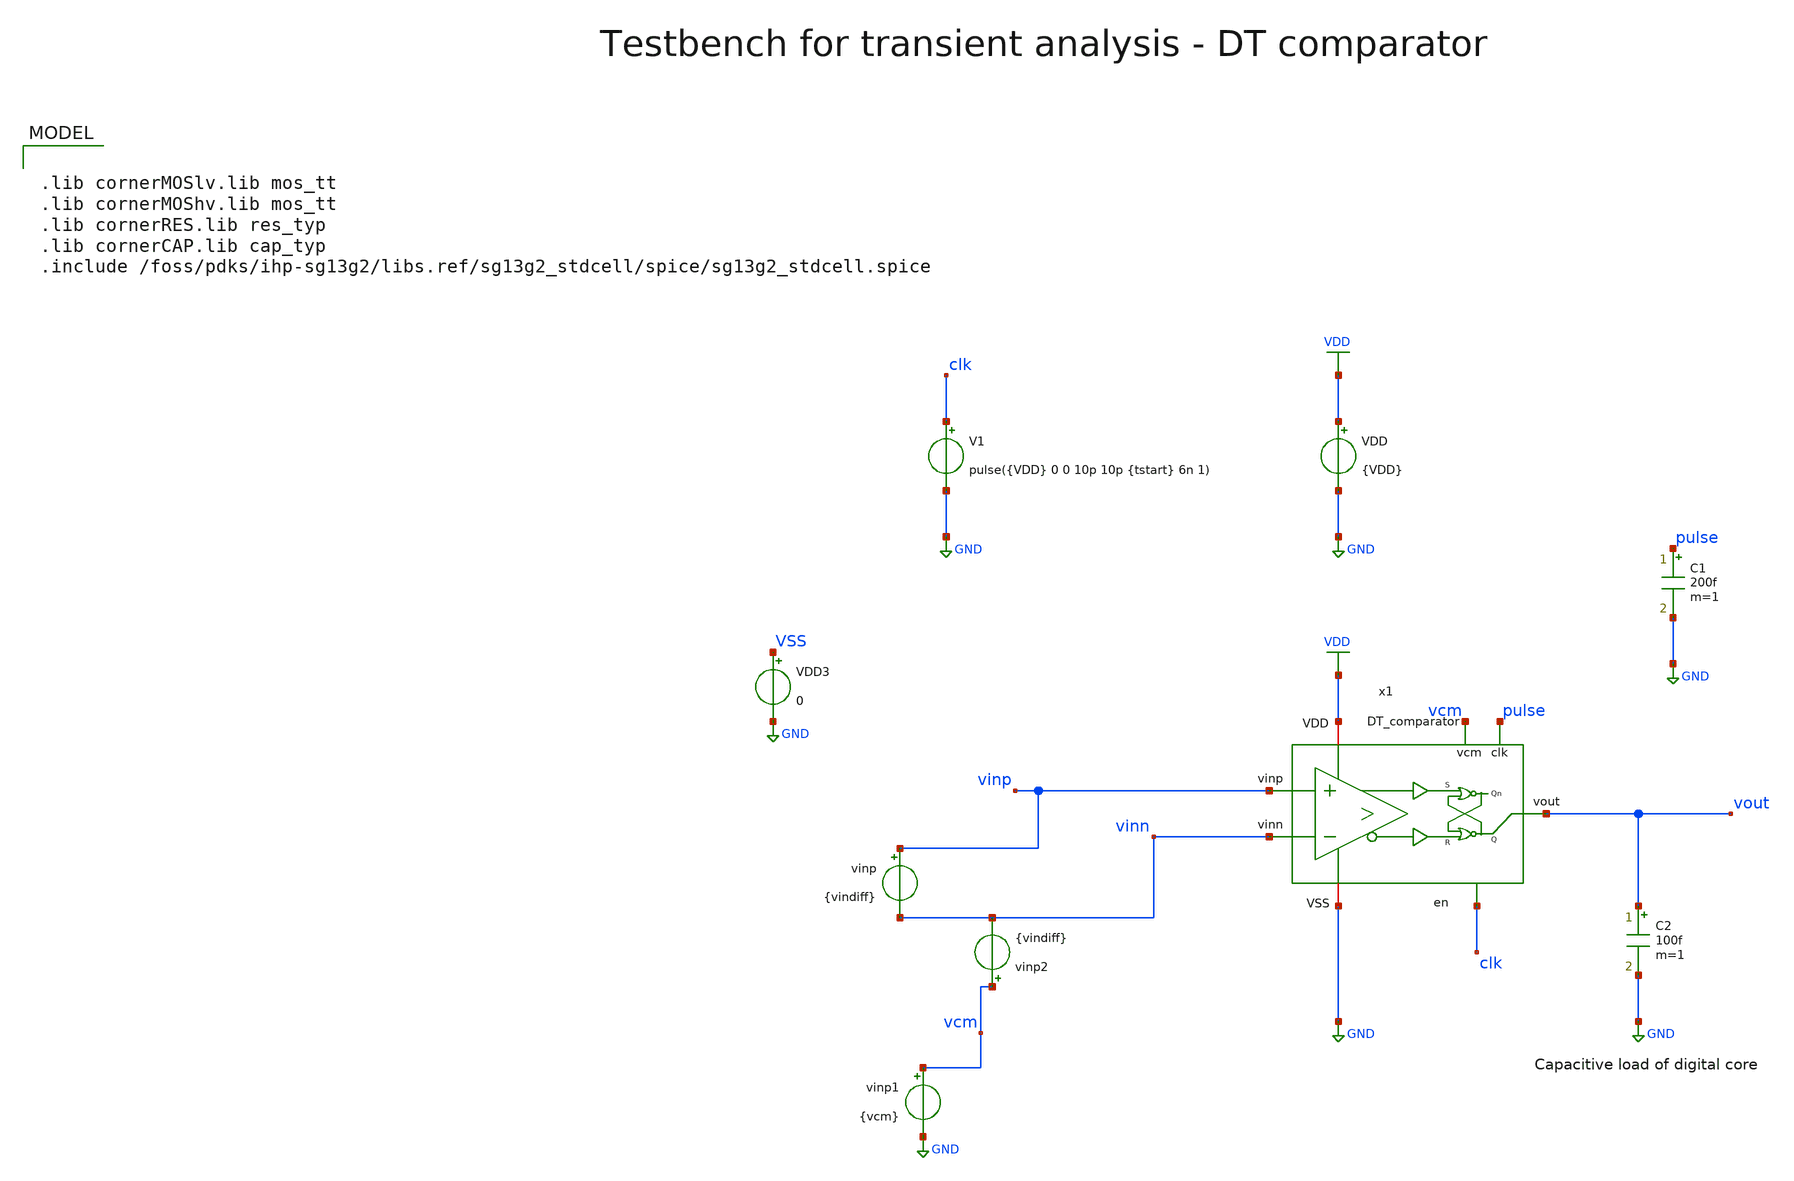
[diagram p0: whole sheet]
** sch_path: xschem/comparator/discrete_time/testbenches/DT_comparator_tb_tran.sch
**.subckt DT_comparator_tb_tran
VDD VDD GND {VDD}
V1 clk GND pulse({VDD} 0 0 10p 10p {tstart} 6n 1)
vinp vinp vinn {vindiff}
C2 vout GND 100f m=1
x1 VDD vinp vout vinn clk GND pulse vcm DT_comparator
VDD3 VSS GND 0
vinp1 vcm GND {vcm}
vinp2 vcm vinn {vindiff}
C1 pulse GND 200f m=1
**** begin user architecture code

.lib cornerMOSlv.lib mos_tt
.lib cornerMOShv.lib mos_tt
.lib cornerRES.lib res_typ
.lib cornerCAP.lib cap_typ
.include /foss/pdks/ihp-sg13g2/libs.ref/sg13g2_stdcell/spice/sg13g2_stdcell.spice



.param vdd=1.8
.param temp=27
.param tstart=2n
.param vindiff = 300u
.param Vcm=0.75

.options savecurrents reltol=1e-3 abstol=1e-12 gmin=1e-15
.ic v(vout) = 0
.control
save all


* Operating Point Analysis
op
remzerovec
write DT_comparator_tb_tran.raw
set appendwrite

* Transient Analysis
* tran 4p 20n
tran 1p 10n
write DT_comparator_tb_tran.raw v(vinp) v(vinn) v(vout)

* Measure vcpp_min & vcpn_min
*let tmeas = 1/fclk
*meas tran vcpp_min FIND qv(x1.x1.vcpp) at=tmeas
*meas tran vcpn_min FIND v(x1.x1.vcpn) at=tmeas

* Measure Propagation Delay
* Time from clock rising edge to 90% VDD of vout

meas tran t_dec1 TRIG v(x1.voutp_buf) VAL=1.62 RISE=1 TARG v(pulse) VAL=0.18 FALL=1
meas tran t_dec2 TRIG v(x1.voutp_buf) VAL=1.62 RISE=2 TARG v(pulse) VAL=0.18 FALL=2
meas tran t_dec3 TRIG v(x1.voutp_buf) VAL=1.62 RISE=3 TARG v(pulse) VAL=0.18 FALL=3

meas tran t_reset1 TRIG pulse VAL=1.62 RISE=2 TARG pulse VAL=0.18 FALL=2
meas tran t_reset2 TRIG pulse VAL=1.62 RISE=3 TARG pulse VAL=0.18 FALL=3
meas tran t_reset3 TRIG pulse VAL=1.62 RISE=4 TARG pulse VAL=0.18 FALL=4

echo Primer tiempo de decision $&t_dec1 s
echo Segundo tiempo de decison $&t_dec3 s


echo Tiempo de espera $&t_reset3 s

* Calculate Energy / Conversion
* i_int in As
* energy_conv in Ws = J
*let N = 1
**let t_conv = tstart + t_dec
*meas tran i_int INTEG i(VDD) from=tstart to=t_conv
*let energy_conv = 1.5 * i_int / N

*let energy_conv_femto = energy_conv * 1e15
*echo Energy / Conversion $&energy_conv_femto fJ/conv

* Plotting

plot i(VDD)
plot v(x1.voutp_buf) {v(x1.voutn_buf)} {v(x1.x6.vx_n) + 4}  {v(pulse) + 8} {v(x1.x6.READY) + 10}
plot v(x1.voutp_comp) {v(x1.voutn_comp)} {v(x1.x6.vx_n) + 4}  {v(x1.x6.vx) + 8} {v(x1.x6.vxs) + 10}
plot x1.voutp_comp pulse x1.voutp_buf x1.x6.ready
* Writing Data
set wr_singlescale
set wr_vecnames
let vs=x1.x1.vs
let vcpp=x1.x1.vcpp
let vcpn=x1.x1.vcpn
let voutp_comp=x1.voutp_comp
let voutn_comp=x1.voutn_comp
wrdata ./../../DT_comparator_tb_tran.txt v(clk) v(vinp) v(vinn) v(vs) v(vcpp) v(vcpn) v(voutp_comp)
+ v(voutn_comp) v(vout)

*quit
.endc

**** end user architecture code
**.ends
.GLOBAL GND
.GLOBAL VDD
.end
